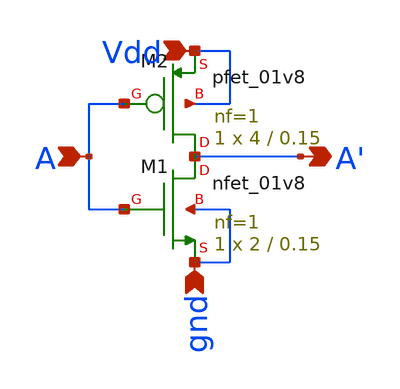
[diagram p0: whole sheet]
** sch_path: extra_stuff/4buff.sch
**.subckt 4buff Vdd A' A gnd
*.ipin Vdd
*.opin A'
*.ipin A
*.ipin gnd
XM1 A' A gnd gnd sky130_fd_pr__nfet_01v8 L=0.15 W=2 nf=1 ad='int((1 + 1)/2) * 2 / 1 * 0.29' as='int((1
+ + 2)/2) * 2 / 1 * 0.29' pd='2*int((1 + 1)/2) * (2 / 1 + 0.29)' ps='2*int((1 + 2)/2) * (2 / 1 + 0.29)' nrd='0.29
+ / 2 ' nrs='0.29 / 2 ' sa=0 sb=0 sd=0 mult=1 m=1
XM2 A' A Vdd Vdd sky130_fd_pr__pfet_01v8 L=0.15 W=4 nf=1 ad='int((1 + 1)/2) * 4 / 1 * 0.29' as='int((1 + 2)/2) * 4 / 1 * 0.29'
+ pd='2*int((1 + 1)/2) * (4 / 1 + 0.29)' ps='2*int((1 + 2)/2) * (4 / 1 + 0.29)' nrd='0.29 / 4 ' nrs='0.29 / 4 '
+ sa=0 sb=0 sd=0 mult=1 m=1
**.ends
.end
